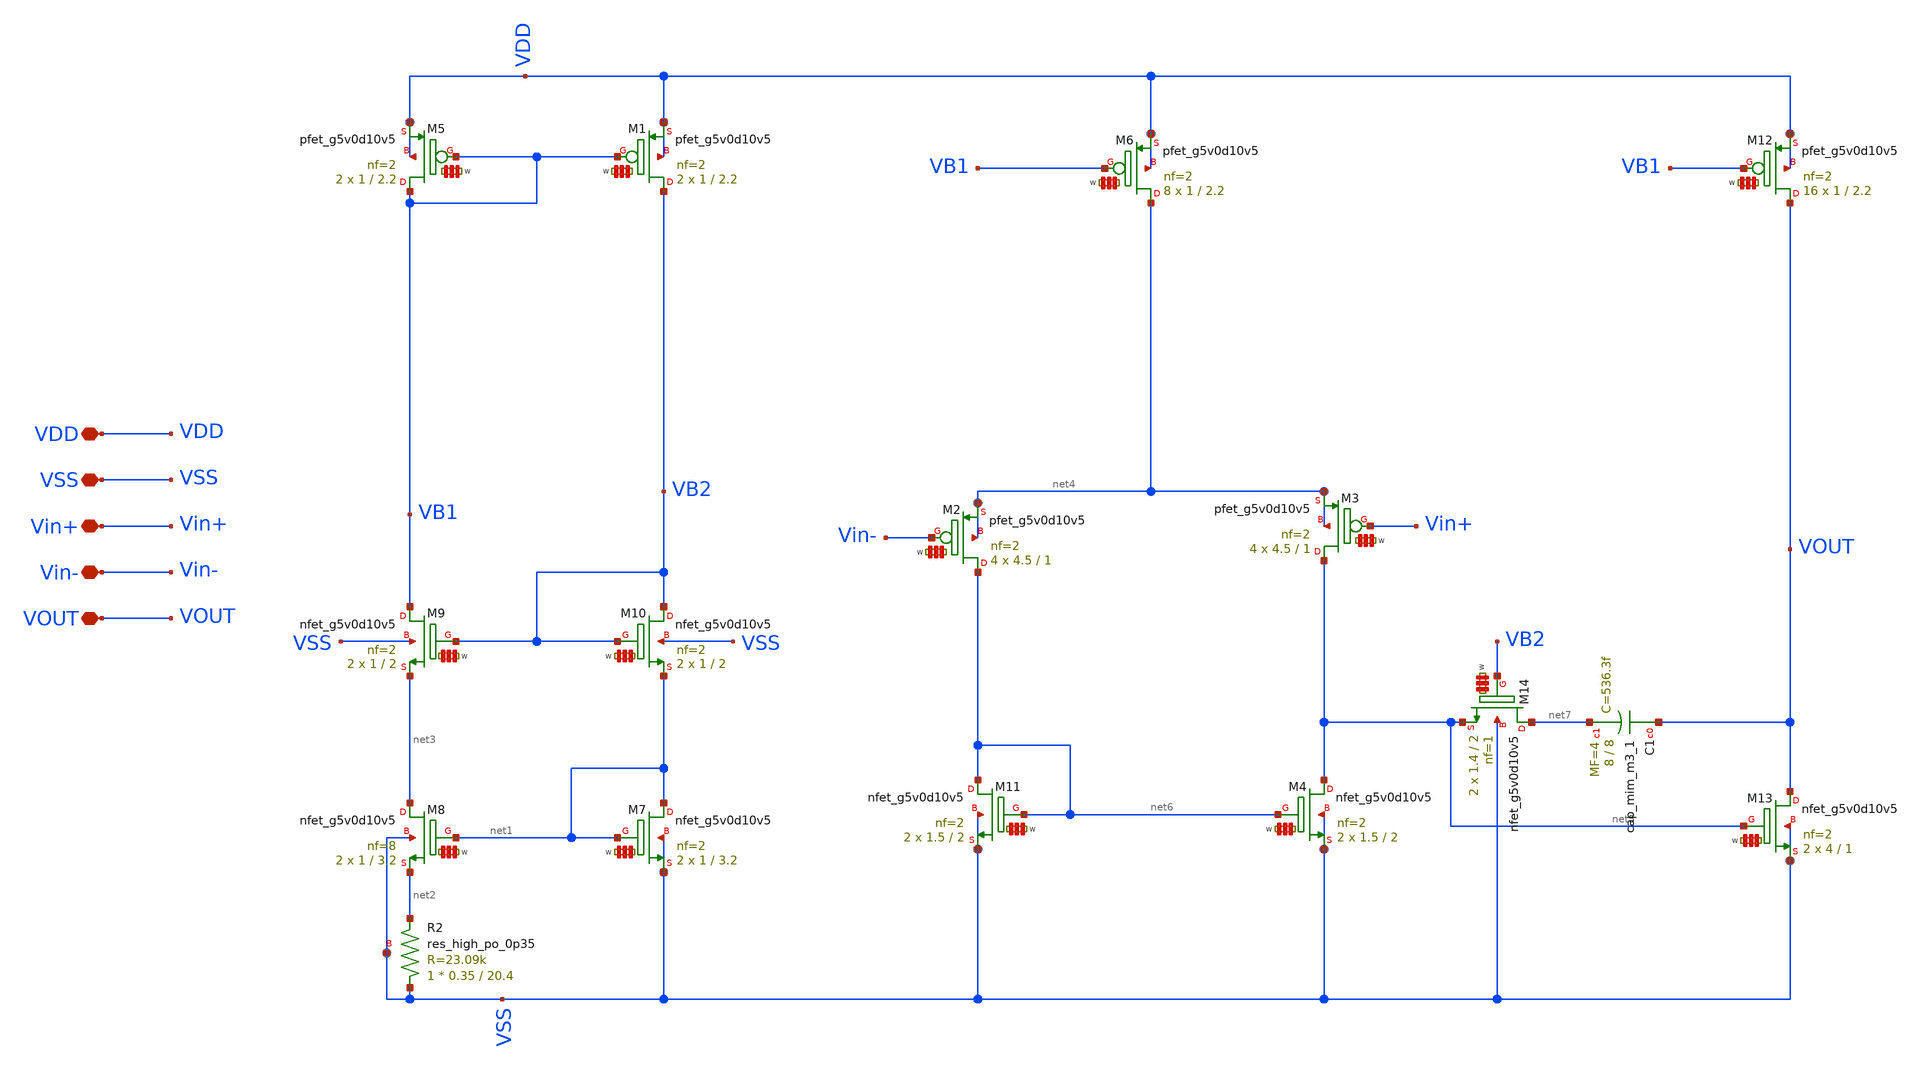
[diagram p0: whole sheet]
** sch_path: my_ip/LIB/Sky130A/Learning/Design_of_Two-Stage_CMOS_Operational_Amplifier_for_Fluorescence_Signal_Processing_5V/amplifier.sch
**.subckt amplifier VDD VSS Vin+ Vin- VOUT
*.iopin VDD
*.iopin VSS
*.iopin Vin+
*.iopin Vin-
*.iopin VOUT
XR2 VSS net2 VSS sky130_fd_pr__res_high_po_0p35 L=20.4 mult=1 m=1
XM7 net1 net1 VSS VSS sky130_fd_pr__nfet_g5v0d10v5 L=3.2 W='1 * 2 ' nf=2 ad='int((nf+1)/2) * W / nf * 0.29'
+ as='int((nf+2)/2) * W / nf * 0.29' pd='2*int((nf+1)/2) * (W / nf + 0.29)' ps='2*int((nf+2)/2) * (W / nf + 0.29)'
+ nrd='0.29 / W ' nrs='0.29 / W ' sa=0 sb=0 sd=0 mult=2 m=2
XM8 net3 net1 net2 VSS sky130_fd_pr__nfet_g5v0d10v5 L=3.2 W='1 * 8 ' nf=8 ad='int((nf+1)/2) * W / nf * 0.29'
+ as='int((nf+2)/2) * W / nf * 0.29' pd='2*int((nf+1)/2) * (W / nf + 0.29)' ps='2*int((nf+2)/2) * (W / nf + 0.29)'
+ nrd='0.29 / W ' nrs='0.29 / W ' sa=0 sb=0 sd=0 mult=2 m=2
XM9 VB1 VB2 net3 VSS sky130_fd_pr__nfet_g5v0d10v5 L=2 W='1 * 2 ' nf=2 ad='int((nf+1)/2) * W / nf * 0.29'
+ as='int((nf+2)/2) * W / nf * 0.29' pd='2*int((nf+1)/2) * (W / nf + 0.29)' ps='2*int((nf+2)/2) * (W / nf + 0.29)'
+ nrd='0.29 / W ' nrs='0.29 / W ' sa=0 sb=0 sd=0 mult=2 m=2
XM10 VB2 VB2 net1 VSS sky130_fd_pr__nfet_g5v0d10v5 L=2 W='1 * 2 ' nf=2 ad='int((nf+1)/2) * W / nf * 0.29'
+ as='int((nf+2)/2) * W / nf * 0.29' pd='2*int((nf+1)/2) * (W / nf + 0.29)' ps='2*int((nf+2)/2) * (W / nf + 0.29)'
+ nrd='0.29 / W ' nrs='0.29 / W ' sa=0 sb=0 sd=0 mult=2 m=2
XM2 net6 Vin- net4 net4 sky130_fd_pr__pfet_g5v0d10v5 L=1 W='4.5 * 2 ' nf=2 ad='int((2 + 1)/2) * 4.5 * 0.29'
+ as='int((2 + 2)/2) * 4.5 * 0.29' pd='2*int((2 + 1)/2) * (4.5 + 0.29)' ps='2*int((2 + 2)/2) * (4.5 + 0.29)'
+ nrd='0.29 / 4.5 / 2 ' nrs='0.29 / 4.5 / 2 ' sa=0 sb=0 sd=0 mult=4 m=4
XM3 net5 Vin+ net4 net4 sky130_fd_pr__pfet_g5v0d10v5 L=1 W='4.5 * 2 ' nf=2 ad='int((2 + 1)/2) * 4.5 * 0.29'
+ as='int((2 + 2)/2) * 4.5 * 0.29' pd='2*int((2 + 1)/2) * (4.5 + 0.29)' ps='2*int((2 + 2)/2) * (4.5 + 0.29)'
+ nrd='0.29 / 4.5 / 2 ' nrs='0.29 / 4.5 / 2 ' sa=0 sb=0 sd=0 mult=4 m=4
XM4 net5 net6 VSS VSS sky130_fd_pr__nfet_g5v0d10v5 L=2 W='1.5 * 2 ' nf=2 ad='int((nf+1)/2) * W / nf * 0.29'
+ as='int((nf+2)/2) * W / nf * 0.29' pd='2*int((nf+1)/2) * (W / nf + 0.29)' ps='2*int((nf+2)/2) * (W / nf + 0.29)'
+ nrd='0.29 / W ' nrs='0.29 / W ' sa=0 sb=0 sd=0 mult=2 m=2
XM11 net6 net6 VSS VSS sky130_fd_pr__nfet_g5v0d10v5 L=2 W='1.5 * 2 ' nf=2 ad='int((nf+1)/2) * W / nf * 0.29'
+ as='int((nf+2)/2) * W / nf * 0.29' pd='2*int((nf+1)/2) * (W / nf + 0.29)' ps='2*int((nf+2)/2) * (W / nf + 0.29)'
+ nrd='0.29 / W ' nrs='0.29 / W ' sa=0 sb=0 sd=0 mult=2 m=2
XM13 VOUT net5 VSS VSS sky130_fd_pr__nfet_g5v0d10v5 L=1 W='4 * 2 ' nf=2 ad='int((nf+1)/2) * W / nf * 0.29'
+ as='int((nf+2)/2) * W / nf * 0.29' pd='2*int((nf+1)/2) * (W / nf + 0.29)' ps='2*int((nf+2)/2) * (W / nf + 0.29)'
+ nrd='0.29 / W ' nrs='0.29 / W ' sa=0 sb=0 sd=0 mult=2 m=2
XM14 net7 VB2 net5 VSS sky130_fd_pr__nfet_g5v0d10v5 L=2 W='1.4 * 1 ' nf=1 ad='int((nf+1)/2) * W / nf * 0.29'
+ as='int((nf+2)/2) * W / nf * 0.29' pd='2*int((nf+1)/2) * (W / nf + 0.29)' ps='2*int((nf+2)/2) * (W / nf + 0.29)'
+ nrd='0.29 / W ' nrs='0.29 / W ' sa=0 sb=0 sd=0 mult=2 m=2
XC1 VOUT net7 sky130_fd_pr__cap_mim_m3_1 W=8 L=8 MF=4 m=4
XM1 VB2 VB1 VDD VDD sky130_fd_pr__pfet_g5v0d10v5 L=2.2 W='1 * 2 ' nf=2 ad='int((2 + 1)/2) * 1 * 0.29'
+ as='int((2 + 2)/2) * 1 * 0.29' pd='2*int((2 + 1)/2) * (1 + 0.29)' ps='2*int((2 + 2)/2) * (1 + 0.29)'
+ nrd='0.29 / 1 / 2 ' nrs='0.29 / 1 / 2 ' sa=0 sb=0 sd=0 mult=2 m=2
XM5 VB1 VB1 VDD VDD sky130_fd_pr__pfet_g5v0d10v5 L=2.2 W='1 * 2 ' nf=2 ad='int((2 + 1)/2) * 1 * 0.29'
+ as='int((2 + 2)/2) * 1 * 0.29' pd='2*int((2 + 1)/2) * (1 + 0.29)' ps='2*int((2 + 2)/2) * (1 + 0.29)'
+ nrd='0.29 / 1 / 2 ' nrs='0.29 / 1 / 2 ' sa=0 sb=0 sd=0 mult=2 m=2
XM6 net4 VB1 VDD VDD sky130_fd_pr__pfet_g5v0d10v5 L=2.2 W='1 * 2 ' nf=2 ad='int((2 + 1)/2) * 1 * 0.29'
+ as='int((2 + 2)/2) * 1 * 0.29' pd='2*int((2 + 1)/2) * (1 + 0.29)' ps='2*int((2 + 2)/2) * (1 + 0.29)'
+ nrd='0.29 / 1 / 2 ' nrs='0.29 / 1 / 2 ' sa=0 sb=0 sd=0 mult=8 m=8
XM12 VOUT VB1 VDD VDD sky130_fd_pr__pfet_g5v0d10v5 L=2.2 W='1 * 2 ' nf=2 ad='int((2 + 1)/2) * 1 * 0.29'
+ as='int((2 + 2)/2) * 1 * 0.29' pd='2*int((2 + 1)/2) * (1 + 0.29)' ps='2*int((2 + 2)/2) * (1 + 0.29)'
+ nrd='0.29 / 1 / 2 ' nrs='0.29 / 1 / 2 ' sa=0 sb=0 sd=0 mult=16 m=16
**.ends
.end
